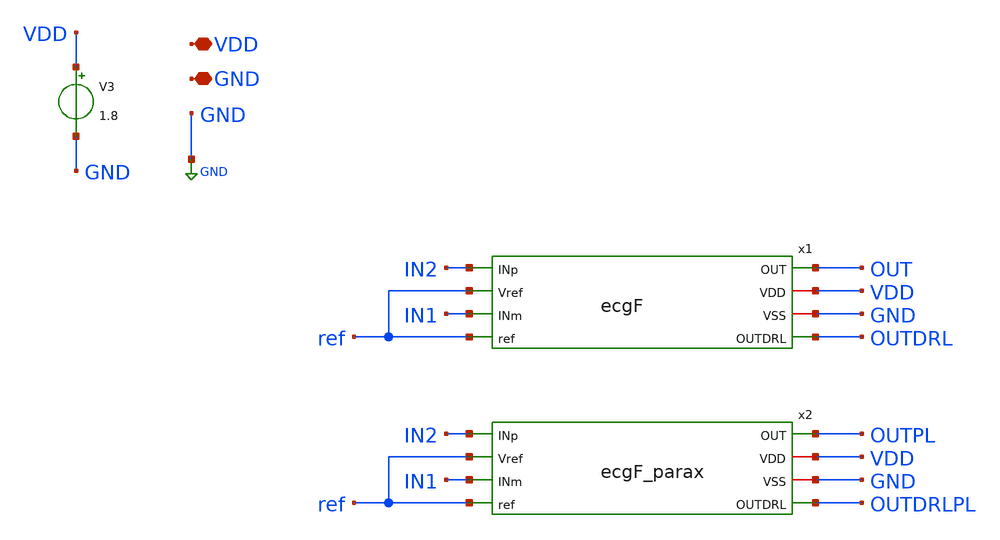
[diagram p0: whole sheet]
** sch_path: xschem/ecgFPL_PWL.sch
**.subckt ecgFPL_PWL VDD GND
*.iopin VDD
*.iopin GND
V3 VDD GND 1.8
x1 IN2 OUT ref IN1 VDD GND ref OUTDRL ecgF
x2 IN2 OUTPL ref IN1 VDD GND ref OUTDRLPL ecgF_parax
**** begin user architecture code
.lib $::SKYWATER_MODELS/sky130.lib.spice tt


 * --- DEFINIZIONE GENERATORI (Aggiornata secondo schema 2026-02-13) ---

* 1. Riferimento DC stabile a 0.9V (Nodo 'ref')
V1 ref GND 0.9

* 2. Generatore di MODO COMUNE (50Hz) connesso tra il punto comune e out_drl
* Nello schema, il morsetto negativo è su out_drl e il positivo va verso gli ingressi
VbiasR3 common_node outdrl dc 0 sin(0 100m 50 10u 0 0)

* 3. Braccio Positivo (ECG / 2) riferito al common_node
VbiasR1 IN1 common_node dc 0 pwl(   0.00 0.00000 0.05 0.00000 0.08 0.00000 0.10 0.00005 0.12
+ 0.000075   0.15 0.00010 0.18 0.000075 0.22 0.00000 0.28 0.00000 0.29 -0.000025   0.30 -0.00005 0.31 0.00035
+ 0.32 0.00075 0.33 0.00035 0.34 -0.00010   0.35 -0.00005 0.36 0.00000 0.40 0.00000 0.48 0.00000 0.52
+ 0.00005   0.56 0.000125 0.60 0.00015 0.64 0.000125 0.68 0.00005 0.75 0.00000   1.00 0.00000 )

* 4. Braccio Negativo (ECG / 2 Invertito) riferito al common_node
VbiasR2 IN2 common_node dc 0 pwl(   0.00 0.00000 0.05 0.00000 0.08 0.00000 0.10 -0.00005 0.12
+ -0.000075   0.15 -0.00010 0.18 -0.000075 0.22 0.00000 0.28 0.00000 0.29 0.000025   0.30 0.00005 0.31 -0.00035
+ 0.32 -0.00075 0.33 -0.00035 0.34 0.00010   0.35 0.00005 0.36 0.00000 0.40 0.00000 0.48 0.00000 0.52
+ -0.00005   0.56 -0.000125 0.60 -0.00015 0.64 -0.000125 0.68 -0.00005 0.75 0.00000   1.00 0.00000 )

* --- CONTROLLO SIMULAZIONE ---
.control
    * Nota: Assicurati che l'ingresso (+) del tuo OTA DRL sia collegato al nodo 'ref' (0.9V)
    * e l'ingresso (-) al modo comune degli elettrodi.
    set wr_vecnames
    save v(IN1) v(IN2) v(common_node) v(outdrl) v(ref) v(out) v(outpl)
    tran 10u 1.1s 0 1m

    * Visualizza come il DRL muove out_drl per annullare il 50Hz nel common_node
    plot v(common_node) v(ref) title 'Modo Comune vs Riferimento 0.9V'
    plot v(out_drl) title 'Uscita Correttiva del DRL'
    plot (v(IN1)-v(IN2)) title 'Segnale ECG Differenziale'
    plot v(out) v(outpl)


.endc



**** end user architecture code
**.ends

* expanding   symbol:  ecgF.sym # of pins=8
** sym_path: xschem/ecgF.sym
** sch_path: xschem/ecgF.sch
.subckt ecgF INp OUT Vref INm VDD VSS ref OUTDRL
*.ipin INp
*.ipin INm
*.opin OUT
*.ipin Vref
*.opin OUTDRL
*.ipin ref
*.iopin VDD
*.iopin VSS
XR3 Vcm net5 VSS sky130_fd_pr__res_high_po_0p35 L=0.6 mult=1 m=1
XR15 Vcm net6 VSS sky130_fd_pr__res_high_po_0p35 L=0.6 mult=1 m=1
XR18 net5 net11 VSS sky130_fd_pr__res_xhigh_po_0p35 L=11 mult=1 m=1
XR20 net10 net9 VSS sky130_fd_pr__res_high_po_5p73 L=2.7 mult=1 m=1
XR17 net12 net1 VSS sky130_fd_pr__res_xhigh_po_0p35 L=11 mult=1 m=1
XR1 net11 net12 VSS sky130_fd_pr__res_xhigh_po_0p35 L=11 mult=1 m=1
XR2 net6 net13 VSS sky130_fd_pr__res_xhigh_po_0p35 L=11 mult=1 m=1
XR21 net14 net2 VSS sky130_fd_pr__res_xhigh_po_0p35 L=11 mult=1 m=1
XR24 net13 net14 VSS sky130_fd_pr__res_xhigh_po_0p35 L=11 mult=1 m=1
XR4 net7 net4 VSS sky130_fd_pr__res_xhigh_po_0p35 L=1.8 mult=1 m=1
XR7 net8 net3 VSS sky130_fd_pr__res_xhigh_po_0p35 L=1.8 mult=1 m=1
XR11 net4 net15 VSS sky130_fd_pr__res_xhigh_po_0p35 L=11 mult=1 m=1
XR19 net16 net17 VSS sky130_fd_pr__res_xhigh_po_0p35 L=11 mult=1 m=1
XR25 net15 net16 VSS sky130_fd_pr__res_xhigh_po_0p35 L=11 mult=1 m=1
XR26 net17 OUT VSS sky130_fd_pr__res_xhigh_po_0p35 L=11 mult=1 m=1
XR12 net3 net18 VSS sky130_fd_pr__res_xhigh_po_0p35 L=11 mult=1 m=1
XR27 net19 net20 VSS sky130_fd_pr__res_xhigh_po_0p35 L=11 mult=1 m=1
XR28 net18 net19 VSS sky130_fd_pr__res_xhigh_po_0p35 L=11 mult=1 m=1
XR29 net20 Vref VSS sky130_fd_pr__res_xhigh_po_0p35 L=11 mult=1 m=1
XC2 net9 OUTDRL sky130_fd_pr__cap_mim_m3_1 W=30 L=30 MF=6 m=6
XR16 net9 net21 VSS sky130_fd_pr__res_xhigh_po_0p35 L=11 mult=1 m=1
XR30 net22 net23 VSS sky130_fd_pr__res_xhigh_po_0p35 L=11 mult=1 m=1
XR32 net21 net22 VSS sky130_fd_pr__res_xhigh_po_0p35 L=11 mult=1 m=1
XR34 net23 OUTDRL VSS sky130_fd_pr__res_xhigh_po_0p35 L=11 mult=1 m=1
x16 Vb VDD VSS Vc2 net1 INp net5 Vc1 Vc OFCB
x1 Vb VDD VSS Vc2 net2 INm net6 Vc1 Vc OFCB
x2 Vb VDD VSS Vc2 net7 net1 net7 Vc1 Vc OFCB
x3 Vb VDD VSS Vc2 net8 net2 net8 Vc1 Vc OFCB
x4 Vb VDD VSS Vc2 OUT net3 net4 Vc1 Vc OFCB
x5 Vb VDD VSS Vc2 net10 Vcm net10 Vc1 Vc OFCB
x6 Vb VDD VSS Vc2 OUTDRL ref net9 Vc1 Vc OFCB
XR35 Vb VDD VSS sky130_fd_pr__res_xhigh_po_0p35 L=5 mult=1 m=1
XR36 VSS Vb VSS sky130_fd_pr__res_xhigh_po_0p35 L=13.2 mult=1 m=1
XR37 Vc VDD VSS sky130_fd_pr__res_xhigh_po_0p35 L=5 mult=1 m=1
XR38 VSS Vc VSS sky130_fd_pr__res_xhigh_po_0p35 L=3.07 mult=1 m=1
XR39 Vc1 VDD VSS sky130_fd_pr__res_xhigh_po_0p35 L=5 mult=1 m=1
XR40 VSS Vc1 VSS sky130_fd_pr__res_xhigh_po_0p35 L=13.2 mult=1 m=1
XR41 Vc2 VDD VSS sky130_fd_pr__res_xhigh_po_0p35 L=5 mult=1 m=1
XR42 VSS Vc2 VSS sky130_fd_pr__res_xhigh_po_0p35 L=1.6 mult=1 m=1
.ends


* expanding   symbol:  ecgF_parax.sym # of pins=8
** sym_path: xschem/ecgF.sym
.include [file normalize ../mag/ecgF.sim.spice]

* expanding   symbol:  OFCB.sym # of pins=9
** sym_path: xschem/OFCB.sym
** sch_path: xschem/OFCB.sch
.subckt OFCB Vb VDD GND Vc2 OUT INp INm Vc1 Vc
*.iopin VDD
*.iopin GND
*.opin OUT
*.ipin INp
*.ipin INm
*.iopin Vc2
*.iopin Vc1
*.iopin Vc
*.iopin Vb
XM11 S Vb VDD VDD sky130_fd_pr__pfet_01v8_lvt L=1 W=60 nf=6 ad='int((nf+1)/2) * W/nf * 0.29' as='int((nf+2)/2) * W/nf * 0.29'
+ pd='2*int((nf+1)/2) * (W/nf + 0.29)' ps='2*int((nf+2)/2) * (W/nf + 0.29)' nrd='0.29 / W' nrs='0.29 / W'
+ sa=0 sb=0 sd=0 mult=2 m=2
XM1 D1 INp S S sky130_fd_pr__pfet_01v8_lvt L=10 W=25 nf=2 ad='int((nf+1)/2) * W/nf * 0.29' as='int((nf+2)/2) * W/nf * 0.29'
+ pd='2*int((nf+1)/2) * (W/nf + 0.29)' ps='2*int((nf+2)/2) * (W/nf + 0.29)' nrd='0.29 / W' nrs='0.29 / W'
+ sa=0 sb=0 sd=0 mult=2 m=2
XM2 D2 INm S S sky130_fd_pr__pfet_01v8_lvt L=10 W=25 nf=2 ad='int((nf+1)/2) * W/nf * 0.29' as='int((nf+2)/2) * W/nf * 0.29'
+ pd='2*int((nf+1)/2) * (W/nf + 0.29)' ps='2*int((nf+2)/2) * (W/nf + 0.29)' nrd='0.29 / W' nrs='0.29 / W'
+ sa=0 sb=0 sd=0 mult=2 m=2
XM3 OUT Vc1 D2 GND sky130_fd_pr__nfet_01v8_lvt L=1 W=4 nf=1 ad='int((nf+1)/2) * W/nf * 0.29' as='int((nf+2)/2) * W/nf * 0.29'
+ pd='2*int((nf+1)/2) * (W/nf + 0.29)' ps='2*int((nf+2)/2) * (W/nf + 0.29)' nrd='0.29 / W' nrs='0.29 / W'
+ sa=0 sb=0 sd=0 mult=1 m=1
XM4 D2 Vc GND GND sky130_fd_pr__nfet_01v8_lvt L=1 W=2.8 nf=1 ad='int((nf+1)/2) * W/nf * 0.29' as='int((nf+2)/2) * W/nf * 0.29'
+ pd='2*int((nf+1)/2) * (W/nf + 0.29)' ps='2*int((nf+2)/2) * (W/nf + 0.29)' nrd='0.29 / W' nrs='0.29 / W'
+ sa=0 sb=0 sd=0 mult=1 m=1
XM5 D1 Vc GND GND sky130_fd_pr__nfet_01v8_lvt L=1 W=2.8 nf=1 ad='int((nf+1)/2) * W/nf * 0.29' as='int((nf+2)/2) * W/nf * 0.29'
+ pd='2*int((nf+1)/2) * (W/nf + 0.29)' ps='2*int((nf+2)/2) * (W/nf + 0.29)' nrd='0.29 / W' nrs='0.29 / W'
+ sa=0 sb=0 sd=0 mult=1 m=1
XM6 G Vc1 D1 GND sky130_fd_pr__nfet_01v8_lvt L=1 W=4 nf=1 ad='int((nf+1)/2) * W/nf * 0.29' as='int((nf+2)/2) * W/nf * 0.29'
+ pd='2*int((nf+1)/2) * (W/nf + 0.29)' ps='2*int((nf+2)/2) * (W/nf + 0.29)' nrd='0.29 / W' nrs='0.29 / W'
+ sa=0 sb=0 sd=0 mult=1 m=1
XM7 G Vc2 D9 D9 sky130_fd_pr__pfet_01v8_lvt L=2.23 W=4 nf=1 ad='int((nf+1)/2) * W/nf * 0.29' as='int((nf+2)/2) * W/nf * 0.29'
+ pd='2*int((nf+1)/2) * (W/nf + 0.29)' ps='2*int((nf+2)/2) * (W/nf + 0.29)' nrd='0.29 / W' nrs='0.29 / W'
+ sa=0 sb=0 sd=0 mult=1 m=1
XM9 D9 G VDD VDD sky130_fd_pr__pfet_01v8_lvt L=2.23 W=3.85 nf=1 ad='int((nf+1)/2) * W/nf * 0.29' as='int((nf+2)/2) * W/nf * 0.29'
+ pd='2*int((nf+1)/2) * (W/nf + 0.29)' ps='2*int((nf+2)/2) * (W/nf + 0.29)' nrd='0.29 / W' nrs='0.29 / W'
+ sa=0 sb=0 sd=0 mult=1 m=1
XM8 D10 G VDD VDD sky130_fd_pr__pfet_01v8_lvt L=2.23 W=3.85 nf=1 ad='int((nf+1)/2) * W/nf * 0.29' as='int((nf+2)/2) * W/nf * 0.29'
+ pd='2*int((nf+1)/2) * (W/nf + 0.29)' ps='2*int((nf+2)/2) * (W/nf + 0.29)' nrd='0.29 / W' nrs='0.29 / W'
+ sa=0 sb=0 sd=0 mult=1 m=1
XM10 OUT Vc2 D10 D10 sky130_fd_pr__pfet_01v8_lvt L=2.23 W=4 nf=1 ad='int((nf+1)/2) * W/nf * 0.29' as='int((nf+2)/2) * W/nf * 0.29'
+ pd='2*int((nf+1)/2) * (W/nf + 0.29)' ps='2*int((nf+2)/2) * (W/nf + 0.29)' nrd='0.29 / W' nrs='0.29 / W'
+ sa=0 sb=0 sd=0 mult=1 m=1
XC1 OUT D1 sky130_fd_pr__cap_mim_m3_1 W=22.4 L=22.4 MF=2 m=2
.ends

.GLOBAL GND
.end
